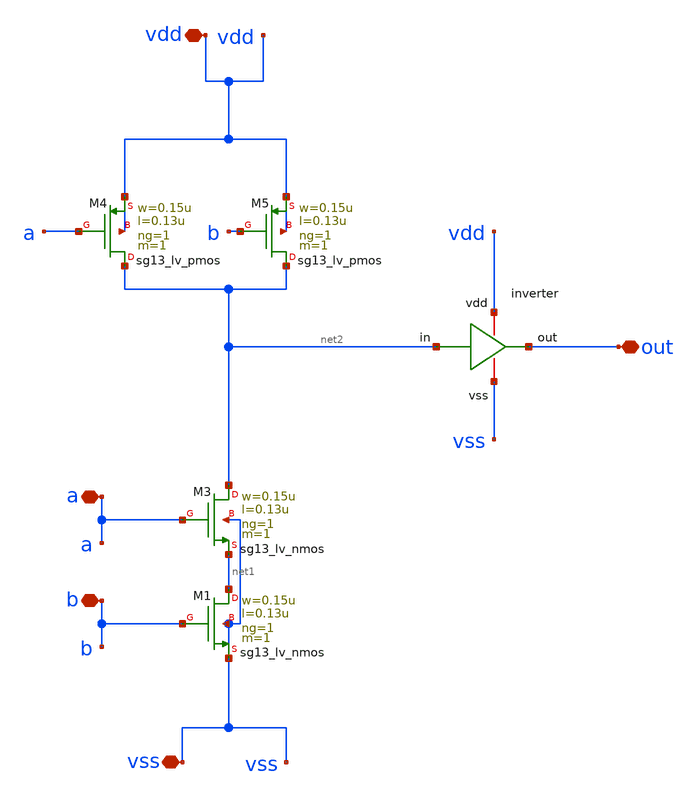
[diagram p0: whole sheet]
** sch_path: design/blocks/andgate/schematic/andgate.sch
**.subckt andgate b a vdd vss out
*.iopin b
*.iopin a
*.iopin vdd
*.iopin vss
*.iopin out
XM1 net1 b vss vss sg13_lv_nmos w=0.15u l=0.13u ng=1 m=1 mm_ok=1
XM4 net2 a vdd vdd sg13_lv_pmos w=0.15u l=0.13u ng=1 m=1 mm_ok=1
x1 vdd out net2 vss inverter
XM3 net2 a net1 vss sg13_lv_nmos w=0.15u l=0.13u ng=1 m=1 mm_ok=1
XM5 net2 b vdd vdd sg13_lv_pmos w=0.15u l=0.13u ng=1 m=1 mm_ok=1
**.ends

* expanding   symbol:  blocks/inverter/schematic/inverter.sym # of pins=4
** sym_path: design/blocks/inverter/schematic/inverter.sym
** sch_path: design/blocks/inverter/schematic/inverter.sch
.subckt inverter vdd out in vss
*.iopin vdd
*.iopin out
*.iopin vss
*.iopin in
XM1 out in vss vss sg13_lv_nmos w=0.75u l=0.15u ng=1 m=1 mm_ok=1
XM2 out in vdd vdd sg13_lv_pmos w=1.5u l=0.15u ng=1 m=1 mm_ok=1
.ends

.end
